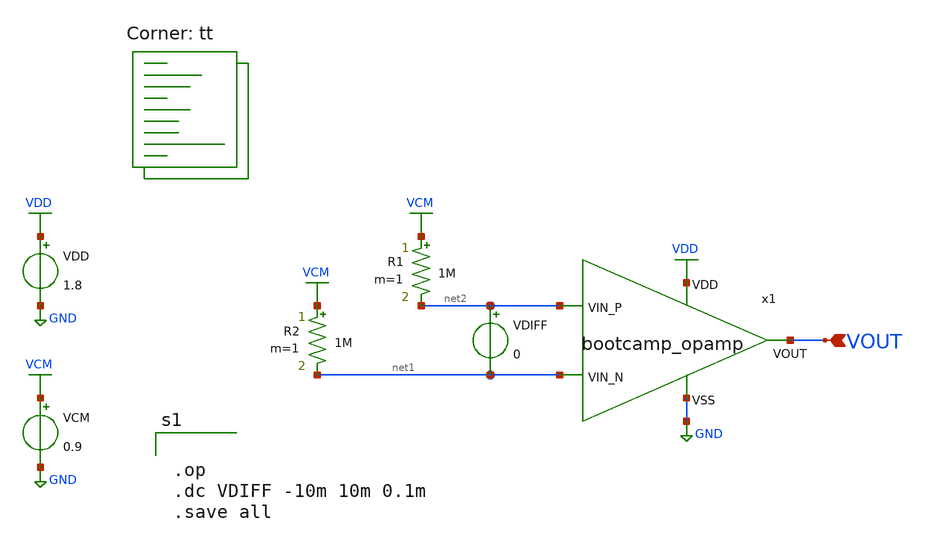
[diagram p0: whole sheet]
** sch_path: analog/schematics/tb_dc_analysis.sch
**.subckt tb_dc_analysis VOUT
*.ipin VOUT
x1 VDD net2 VOUT net1 GND bootcamp_opamp
R1 VCM net2 1M m=1
R2 VCM net1 1M m=1
VDD VDD GND 1.8
VCM VCM GND 0.9
VDIFF net2 net1 0
**** begin user architecture code


.op
.dc VDIFF -10m 10m 0.1m
.save all


.lib $::SKYWATER_MODELS/sky130.lib.spice tt
**** end user architecture code
**.ends

* expanding   symbol:  bootcamp_opamp.sym # of pins=5
** sym_path: analog/symbols/bootcamp_opamp.sym
** sch_path: analog/symbols/bootcamp_opamp.sch
.subckt bootcamp_opamp VDD VIN_P VOUT VIN_N VSS
*.ipin VIN_P
*.ipin VIN_N
*.ipin VDD
*.ipin VOUT
*.ipin VSS
XM1 net1 VIN_P net2 VSS sky130_fd_pr__nfet_01v8 L=0.15 W=1 nf=1 ad='int((nf+1)/2) * W/nf * 0.29' as='int((nf+2)/2) * W/nf * 0.29'
+ pd='2*int((nf+1)/2) * (W/nf + 0.29)' ps='2*int((nf+2)/2) * (W/nf + 0.29)' nrd='0.29 / W' nrs='0.29 / W'
+ sa=0 sb=0 sd=0 mult=1 m=1
XM2 VOUT VIN_N net2 VSS sky130_fd_pr__nfet_01v8 L=0.15 W=1 nf=1 ad='int((nf+1)/2) * W/nf * 0.29' as='int((nf+2)/2) * W/nf * 0.29'
+ pd='2*int((nf+1)/2) * (W/nf + 0.29)' ps='2*int((nf+2)/2) * (W/nf + 0.29)' nrd='0.29 / W' nrs='0.29 / W'
+ sa=0 sb=0 sd=0 mult=1 m=1
XM3 net1 net1 VDD VDD sky130_fd_pr__pfet_01v8 L=0.15 W=1 nf=1 ad='int((nf+1)/2) * W/nf * 0.29' as='int((nf+2)/2) * W/nf * 0.29'
+ pd='2*int((nf+1)/2) * (W/nf + 0.29)' ps='2*int((nf+2)/2) * (W/nf + 0.29)' nrd='0.29 / W' nrs='0.29 / W'
+ sa=0 sb=0 sd=0 mult=1 m=1
XM4 VOUT net1 VDD VDD sky130_fd_pr__pfet_01v8 L=0.15 W=1 nf=1 ad='int((nf+1)/2) * W/nf * 0.29' as='int((nf+2)/2) * W/nf * 0.29'
+ pd='2*int((nf+1)/2) * (W/nf + 0.29)' ps='2*int((nf+2)/2) * (W/nf + 0.29)' nrd='0.29 / W' nrs='0.29 / W'
+ sa=0 sb=0 sd=0 mult=1 m=1
XM5 net2 net3 VSS VSS sky130_fd_pr__nfet_01v8 L=0.15 W=1 nf=1 ad='int((nf+1)/2) * W/nf * 0.29' as='int((nf+2)/2) * W/nf * 0.29'
+ pd='2*int((nf+1)/2) * (W/nf + 0.29)' ps='2*int((nf+2)/2) * (W/nf + 0.29)' nrd='0.29 / W' nrs='0.29 / W'
+ sa=0 sb=0 sd=0 mult=1 m=1
XM6 VOUT VOUT VDD VDD sky130_fd_pr__pfet_01v8 L=0.15 W=1 nf=1 ad='int((nf+1)/2) * W/nf * 0.29' as='int((nf+2)/2) * W/nf * 0.29'
+ pd='2*int((nf+1)/2) * (W/nf + 0.29)' ps='2*int((nf+2)/2) * (W/nf + 0.29)' nrd='0.29 / W' nrs='0.29 / W'
+ sa=0 sb=0 sd=0 mult=1 m=1
XM7 VOUT net3 VSS VSS sky130_fd_pr__nfet_01v8 L=0.15 W=1 nf=1 ad='int((nf+1)/2) * W/nf * 0.29' as='int((nf+2)/2) * W/nf * 0.29'
+ pd='2*int((nf+1)/2) * (W/nf + 0.29)' ps='2*int((nf+2)/2) * (W/nf + 0.29)' nrd='0.29 / W' nrs='0.29 / W'
+ sa=0 sb=0 sd=0 mult=1 m=1
C1 VOUT GND 1p m=1
XM8 net3 net3 VSS VSS sky130_fd_pr__nfet_01v8 L=0.15 W=1 nf=1 ad='int((nf+1)/2) * W/nf * 0.29' as='int((nf+2)/2) * W/nf * 0.29'
+ pd='2*int((nf+1)/2) * (W/nf + 0.29)' ps='2*int((nf+2)/2) * (W/nf + 0.29)' nrd='0.29 / W' nrs='0.29 / W'
+ sa=0 sb=0 sd=0 mult=1 m=1
R1 VDD net3 1k m=1
.ends

.GLOBAL GND
.GLOBAL VDD
.GLOBAL VCM
.end
